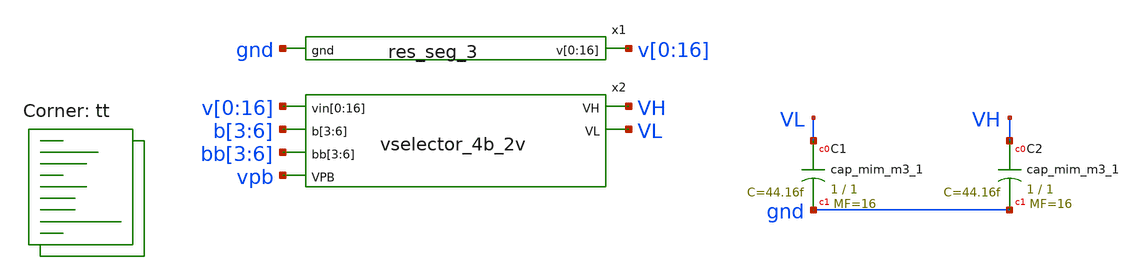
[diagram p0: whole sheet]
** sch_path: xschem/res_seg_3_v2-tb.sch
**.subckt res_seg_3_v2-tb
x1 v[0] v[1] v[2] v[3] v[4] v[5] v[6] v[7] v[8] v[9] v[10] v[11] v[12] v[13] v[14] v[15] v[16] gnd
+ res_seg_3
XC1 VL gnd sky130_fd_pr__cap_mim_m3_1 W=1 L=1 MF=16 m=16
XC2 VH gnd sky130_fd_pr__cap_mim_m3_1 W=1 L=1 MF=16 m=16
x2 v[0] v[1] v[2] v[3] v[4] v[5] v[6] v[7] v[8] v[9] v[10] v[11] v[12] v[13] v[14] v[15] v[16] b[3]
+ b[4] b[5] b[6] bb[3] bb[4] bb[5] bb[6] VH VL vpb vselector_4b_2v
**** begin user architecture code



  .option wnflag=1
  .option safecurrents
  ********************Static Voltage Sources***************************
  Vddh vddh gnd dc 5.5
  Vpb  vpb  gnd dc 5.5

  V8 v[16] gnd dc 4.7190
  v0 v[0] gnd dc 4.0164
  ********************Dynamic Voltage Sources***************************
  *******Calculation**********
  .param base_f=100e3 base_t={1/base_f} base_th={base_t/2} base_d={base_th}
  .param b3_th={base_th} b3_t={b3_th*2}
  .param b4_th={b3_th*2} b4_t={b4_th*2}
  .param b5_th={b4_th*2} b5_t={b5_th*2}
  .param b6_th={b5_th*2} b6_t={b6_th*2}
  *******Signals**********
  .param vhi=1.8
  Vb3  b[3]  gnd pulse({vhi} 0 {base_d} 1n 1n {b3_th} {b3_t})
  Vb4  b[4]  gnd pulse({vhi} 0 {base_d} 1n 1n {b4_th} {b4_t})
  Vb5  b[5]  gnd pulse({vhi} 0 {base_d} 1n 1n {b5_th} {b5_t})
  Vb6  b[6]  gnd pulse({vhi} 0 {base_d} 1n 1n {b6_th} {b6_t})

  Vbb3  bb[3]  gnd pulse(0 {vhi} {base_d} 1n 1n {b3_th} {b3_t})
  Vbb4  bb[4]  gnd pulse(0 {vhi} {base_d} 1n 1n {b4_th} {b4_t})
  Vbb5  bb[5]  gnd pulse(0 {vhi} {base_d} 1n 1n {b5_th} {b5_t})
  Vbb6  bb[6]  gnd pulse(0 {vhi} {base_d} 1n 1n {b6_th} {b6_t})
  ********************Simulation Commands*****************************
  .control
     reset
     save all
     tran 1n 100u
     write res_seg_3_v2-tb.raw
     set appendwrite
*    quit 0
  .endc



.lib $::SKYWATER_MODELS/sky130.lib.spice tt
**** end user architecture code
**.ends

* expanding   symbol:  res_seg_3.sym # of pins=2
** sym_path: xschem/res_seg_3.sym
** sch_path: xschem/res_seg_3.sch
.subckt res_seg_3 v[0] v[1] v[2] v[3] v[4] v[5] v[6] v[7] v[8] v[9] v[10] v[11] v[12] v[13] v[14]
+ v[15] v[16] gnd
*.opin v[0],v[1],v[2],v[3],v[4],v[5],v[6],v[7],v[8],v[9],v[10],v[11],v[12],v[13],v[14],v[15],v[16]
*.ipin gnd
XR1 v[0] v[1] gnd sky130_fd_pr__res_xhigh_po_0p35 L=0.5555 mult=1 m=1
XR2 v[1] v[2] gnd sky130_fd_pr__res_xhigh_po_0p35 L=0.5726 mult=1 m=1
XR3 v[2] v[3] gnd sky130_fd_pr__res_xhigh_po_0p35 L=0.5811 mult=1 m=1
XR4 v[3] v[4] gnd sky130_fd_pr__res_xhigh_po_0p35 L=0.5897 mult=1 m=1
XR5 v[4] v[5] gnd sky130_fd_pr__res_xhigh_po_0p35 L=0.6153 mult=1 m=1
XR6 v[5] v[6] gnd sky130_fd_pr__res_xhigh_po_0p35 L=0.6238 mult=1 m=1
XR7 v[6] v[7] gnd sky130_fd_pr__res_xhigh_po_0p35 L=0.6409 mult=1 m=1
XR8 v[7] v[8] gnd sky130_fd_pr__res_xhigh_po_0p35 L=0.6666 mult=1 m=1
XR9 v[8] v[9] gnd sky130_fd_pr__res_xhigh_po_0p35 L=0.6837 mult=1 m=1
XR10 v[9] v[10] gnd sky130_fd_pr__res_xhigh_po_0p35 L=0.7093 mult=1 m=1
XR11 v[10] v[11] gnd sky130_fd_pr__res_xhigh_po_0p35 L=0.7264 mult=1 m=1
XR12 v[11] v[12] gnd sky130_fd_pr__res_xhigh_po_0p35 L=0.7691 mult=1 m=1
XR13 v[12] v[13] gnd sky130_fd_pr__res_xhigh_po_0p35 L=0.7948 mult=1 m=1
XR14 v[13] v[14] gnd sky130_fd_pr__res_xhigh_po_0p35 L=0.8375 mult=1 m=1
XR15 v[14] v[15] gnd sky130_fd_pr__res_xhigh_po_0p35 L=0.8802 mult=1 m=1
XR16 v[15] v[16] gnd sky130_fd_pr__res_xhigh_po_0p35 L=0.9315 mult=1 m=1
.ends


* expanding   symbol:  vselector_4b_2v.sym # of pins=6
** sym_path: xschem/vselector_4b_2v.sym
** sch_path: xschem/vselector_4b_2v.sch
.subckt vselector_4b_2v vin[0] vin[1] vin[2] vin[3] vin[4] vin[5] vin[6] vin[7] vin[8] vin[9]
+ vin[10] vin[11] vin[12] vin[13] vin[14] vin[15] vin[16] b[3] b[4] b[5] b[6] bb[3] bb[4] bb[5] bb[6] VH VL
+ VPB
*.ipin
*+ vin[0],vin[1],vin[2],vin[3],vin[4],vin[5],vin[6],vin[7],vin[8],vin[9],vin[10],vin[11],vin[12],vin[13],vin[14],vin[15],vin[16]
*.opin VH
*.ipin VPB
*.ipin b[3],b[4],b[5],b[6]
*.opin VL
*.ipin bb[3],bb[4],bb[5],bb[6]
x1 vin[0] vin[1] vin[2] vin[3] vin[4] vin[5] vin[6] vin[7] vin[8] b[6] v1[0] v1[1] v1[2] v1[3] v1[4]
+ v1[5] v1[6] v1[7] v1[8] VPB switch_pmos_1g_9o
x2 vin[8] vin[9] vin[10] vin[11] vin[12] vin[13] vin[14] vin[15] vin[16] bb[6] v1[0] v1[1] v1[2]
+ v1[3] v1[4] v1[5] v1[6] v1[7] v1[8] VPB switch_pmos_1g_9o
x3 v1[0] v1[1] v1[2] v1[3] v1[4] b[5] v2[0] v2[1] v2[2] v2[3] v2[4] VPB switch_pmos_1g_5o
x4 v1[4] v1[5] v1[6] v1[7] v1[8] bb[5] v2[0] v2[1] v2[2] v2[3] v2[4] VPB switch_pmos_1g_5o
x5 v2[0] v2[1] v2[2] b[4] v3[0] v3[1] v3[2] VPB switch_pmos_1g_3o
x6 v2[2] v2[3] v2[4] bb[4] v3[0] v3[1] v3[2] VPB switch_pmos_1g_3o
x7 v3[0] v3[1] b[3] VH VL VPB switch_pmos_1g_2o
x8 v3[1] v3[2] bb[3] VH VL VPB switch_pmos_1g_2o
.ends


* expanding   symbol:  switch_pmos_1g_9o.sym # of pins=4
** sym_path: xschem/switch_pmos_1g_9o.sym
** sch_path: xschem/switch_pmos_1g_9o.sch
.subckt switch_pmos_1g_9o vin[0] vin[1] vin[2] vin[3] vin[4] vin[5] vin[6] vin[7] vin[8] DIN vout[0]
+ vout[1] vout[2] vout[3] vout[4] vout[5] vout[6] vout[7] vout[8] VPB
*.ipin vin[0],vin[1],vin[2],vin[3],vin[4],vin[5],vin[6],vin[7],vin[8]
*.opin vout[0],vout[1],vout[2],vout[3],vout[4],vout[5],vout[6],vout[7],vout[8]
*.ipin VPB
*.ipin DIN
.param wp=0.42 wn=0.42 l=0.5

XM1 vout[0] DIN vin[0] VPB sky130_fd_pr__pfet_g5v0d10v5 L=l W=wp nf=1 ad='int((nf+1)/2) * W/nf * 0.29'
+ as='int((nf+2)/2) * W/nf * 0.29' pd='2*int((nf+1)/2) * (W/nf + 0.29)' ps='2*int((nf+2)/2) * (W/nf + 0.29)'
+ nrd='0.29 / W' nrs='0.29 / W' sa=0 sb=0 sd=0 mult=1 m=1
XM2 vout[1] DIN vin[1] VPB sky130_fd_pr__pfet_g5v0d10v5 L=l W=wp nf=1 ad='int((nf+1)/2) * W/nf * 0.29'
+ as='int((nf+2)/2) * W/nf * 0.29' pd='2*int((nf+1)/2) * (W/nf + 0.29)' ps='2*int((nf+2)/2) * (W/nf + 0.29)'
+ nrd='0.29 / W' nrs='0.29 / W' sa=0 sb=0 sd=0 mult=1 m=1
XM3 vout[2] DIN vin[2] VPB sky130_fd_pr__pfet_g5v0d10v5 L=l W=wp nf=1 ad='int((nf+1)/2) * W/nf * 0.29'
+ as='int((nf+2)/2) * W/nf * 0.29' pd='2*int((nf+1)/2) * (W/nf + 0.29)' ps='2*int((nf+2)/2) * (W/nf + 0.29)'
+ nrd='0.29 / W' nrs='0.29 / W' sa=0 sb=0 sd=0 mult=1 m=1
XM4 vout[3] DIN vin[3] VPB sky130_fd_pr__pfet_g5v0d10v5 L=l W=wp nf=1 ad='int((nf+1)/2) * W/nf * 0.29'
+ as='int((nf+2)/2) * W/nf * 0.29' pd='2*int((nf+1)/2) * (W/nf + 0.29)' ps='2*int((nf+2)/2) * (W/nf + 0.29)'
+ nrd='0.29 / W' nrs='0.29 / W' sa=0 sb=0 sd=0 mult=1 m=1
XM5 vout[4] DIN vin[4] VPB sky130_fd_pr__pfet_g5v0d10v5 L=l W=wp nf=1 ad='int((nf+1)/2) * W/nf * 0.29'
+ as='int((nf+2)/2) * W/nf * 0.29' pd='2*int((nf+1)/2) * (W/nf + 0.29)' ps='2*int((nf+2)/2) * (W/nf + 0.29)'
+ nrd='0.29 / W' nrs='0.29 / W' sa=0 sb=0 sd=0 mult=1 m=1
XM6 vout[5] DIN vin[5] VPB sky130_fd_pr__pfet_g5v0d10v5 L=l W=wp nf=1 ad='int((nf+1)/2) * W/nf * 0.29'
+ as='int((nf+2)/2) * W/nf * 0.29' pd='2*int((nf+1)/2) * (W/nf + 0.29)' ps='2*int((nf+2)/2) * (W/nf + 0.29)'
+ nrd='0.29 / W' nrs='0.29 / W' sa=0 sb=0 sd=0 mult=1 m=1
XM7 vout[6] DIN vin[6] VPB sky130_fd_pr__pfet_g5v0d10v5 L=l W=wp nf=1 ad='int((nf+1)/2) * W/nf * 0.29'
+ as='int((nf+2)/2) * W/nf * 0.29' pd='2*int((nf+1)/2) * (W/nf + 0.29)' ps='2*int((nf+2)/2) * (W/nf + 0.29)'
+ nrd='0.29 / W' nrs='0.29 / W' sa=0 sb=0 sd=0 mult=1 m=1
XM8 vout[7] DIN vin[7] VPB sky130_fd_pr__pfet_g5v0d10v5 L=l W=wp nf=1 ad='int((nf+1)/2) * W/nf * 0.29'
+ as='int((nf+2)/2) * W/nf * 0.29' pd='2*int((nf+1)/2) * (W/nf + 0.29)' ps='2*int((nf+2)/2) * (W/nf + 0.29)'
+ nrd='0.29 / W' nrs='0.29 / W' sa=0 sb=0 sd=0 mult=1 m=1
XM9 vout[8] DIN vin[8] VPB sky130_fd_pr__pfet_g5v0d10v5 L=l W=wp nf=1 ad='int((nf+1)/2) * W/nf * 0.29'
+ as='int((nf+2)/2) * W/nf * 0.29' pd='2*int((nf+1)/2) * (W/nf + 0.29)' ps='2*int((nf+2)/2) * (W/nf + 0.29)'
+ nrd='0.29 / W' nrs='0.29 / W' sa=0 sb=0 sd=0 mult=1 m=1
.ends


* expanding   symbol:  switch_pmos_1g_5o.sym # of pins=4
** sym_path: xschem/switch_pmos_1g_5o.sym
** sch_path: xschem/switch_pmos_1g_5o.sch
.subckt switch_pmos_1g_5o vin[0] vin[1] vin[2] vin[3] vin[4] DIN vout[0] vout[1] vout[2] vout[3]
+ vout[4] VPB
*.ipin vin[0],vin[1],vin[2],vin[3],vin[4]
*.opin vout[0],vout[1],vout[2],vout[3],vout[4]
*.ipin VPB
*.ipin DIN
.param wp=0.42 wn=0.42 l=0.5

XM1 vout[0] DIN vin[0] VPB sky130_fd_pr__pfet_g5v0d10v5 L=l W=wp nf=1 ad='int((nf+1)/2) * W/nf * 0.29'
+ as='int((nf+2)/2) * W/nf * 0.29' pd='2*int((nf+1)/2) * (W/nf + 0.29)' ps='2*int((nf+2)/2) * (W/nf + 0.29)'
+ nrd='0.29 / W' nrs='0.29 / W' sa=0 sb=0 sd=0 mult=1 m=1
XM2 vout[1] DIN vin[1] VPB sky130_fd_pr__pfet_g5v0d10v5 L=l W=wp nf=1 ad='int((nf+1)/2) * W/nf * 0.29'
+ as='int((nf+2)/2) * W/nf * 0.29' pd='2*int((nf+1)/2) * (W/nf + 0.29)' ps='2*int((nf+2)/2) * (W/nf + 0.29)'
+ nrd='0.29 / W' nrs='0.29 / W' sa=0 sb=0 sd=0 mult=1 m=1
XM3 vout[2] DIN vin[2] VPB sky130_fd_pr__pfet_g5v0d10v5 L=l W=wp nf=1 ad='int((nf+1)/2) * W/nf * 0.29'
+ as='int((nf+2)/2) * W/nf * 0.29' pd='2*int((nf+1)/2) * (W/nf + 0.29)' ps='2*int((nf+2)/2) * (W/nf + 0.29)'
+ nrd='0.29 / W' nrs='0.29 / W' sa=0 sb=0 sd=0 mult=1 m=1
XM4 vout[3] DIN vin[3] VPB sky130_fd_pr__pfet_g5v0d10v5 L=l W=wp nf=1 ad='int((nf+1)/2) * W/nf * 0.29'
+ as='int((nf+2)/2) * W/nf * 0.29' pd='2*int((nf+1)/2) * (W/nf + 0.29)' ps='2*int((nf+2)/2) * (W/nf + 0.29)'
+ nrd='0.29 / W' nrs='0.29 / W' sa=0 sb=0 sd=0 mult=1 m=1
XM5 vout[4] DIN vin[4] VPB sky130_fd_pr__pfet_g5v0d10v5 L=l W=wp nf=1 ad='int((nf+1)/2) * W/nf * 0.29'
+ as='int((nf+2)/2) * W/nf * 0.29' pd='2*int((nf+1)/2) * (W/nf + 0.29)' ps='2*int((nf+2)/2) * (W/nf + 0.29)'
+ nrd='0.29 / W' nrs='0.29 / W' sa=0 sb=0 sd=0 mult=1 m=1
.ends


* expanding   symbol:  switch_pmos_1g_3o.sym # of pins=4
** sym_path: xschem/switch_pmos_1g_3o.sym
** sch_path: xschem/switch_pmos_1g_3o.sch
.subckt switch_pmos_1g_3o vin[0] vin[1] vin[2] DIN vout[0] vout[1] vout[2] VPB
*.ipin vin[0],vin[1],vin[2]
*.opin vout[0],vout[1],vout[2]
*.ipin VPB
*.ipin DIN
.param wp=0.42 wn=0.42 l=0.5

XM1 vout[0] DIN vin[0] VPB sky130_fd_pr__pfet_g5v0d10v5 L=l W=wp nf=1 ad='int((nf+1)/2) * W/nf * 0.29'
+ as='int((nf+2)/2) * W/nf * 0.29' pd='2*int((nf+1)/2) * (W/nf + 0.29)' ps='2*int((nf+2)/2) * (W/nf + 0.29)'
+ nrd='0.29 / W' nrs='0.29 / W' sa=0 sb=0 sd=0 mult=1 m=1
XM2 vout[1] DIN vin[1] VPB sky130_fd_pr__pfet_g5v0d10v5 L=l W=wp nf=1 ad='int((nf+1)/2) * W/nf * 0.29'
+ as='int((nf+2)/2) * W/nf * 0.29' pd='2*int((nf+1)/2) * (W/nf + 0.29)' ps='2*int((nf+2)/2) * (W/nf + 0.29)'
+ nrd='0.29 / W' nrs='0.29 / W' sa=0 sb=0 sd=0 mult=1 m=1
XM3 vout[2] DIN vin[2] VPB sky130_fd_pr__pfet_g5v0d10v5 L=l W=wp nf=1 ad='int((nf+1)/2) * W/nf * 0.29'
+ as='int((nf+2)/2) * W/nf * 0.29' pd='2*int((nf+1)/2) * (W/nf + 0.29)' ps='2*int((nf+2)/2) * (W/nf + 0.29)'
+ nrd='0.29 / W' nrs='0.29 / W' sa=0 sb=0 sd=0 mult=1 m=1
.ends


* expanding   symbol:  switch_pmos_1g_2o.sym # of pins=5
** sym_path: xschem/switch_pmos_1g_2o.sym
** sch_path: xschem/switch_pmos_1g_2o.sch
.subckt switch_pmos_1g_2o vin[0] vin[1] DIN VH VL VPB
*.ipin vin[0],vin[1]
*.opin VH
*.ipin VPB
*.ipin DIN
*.opin VL
.param wp=0.42 wn=0.42 l=0.5

XM1 VL DIN vin[0] VPB sky130_fd_pr__pfet_g5v0d10v5 L=l W=wp nf=1 ad='int((nf+1)/2) * W/nf * 0.29' as='int((nf+2)/2) * W/nf * 0.29'
+ pd='2*int((nf+1)/2) * (W/nf + 0.29)' ps='2*int((nf+2)/2) * (W/nf + 0.29)' nrd='0.29 / W' nrs='0.29 / W'
+ sa=0 sb=0 sd=0 mult=1 m=1
XM2 VH DIN vin[1] VPB sky130_fd_pr__pfet_g5v0d10v5 L=l W=wp nf=1 ad='int((nf+1)/2) * W/nf * 0.29' as='int((nf+2)/2) * W/nf * 0.29'
+ pd='2*int((nf+1)/2) * (W/nf + 0.29)' ps='2*int((nf+2)/2) * (W/nf + 0.29)' nrd='0.29 / W' nrs='0.29 / W'
+ sa=0 sb=0 sd=0 mult=1 m=1
.ends

.end
